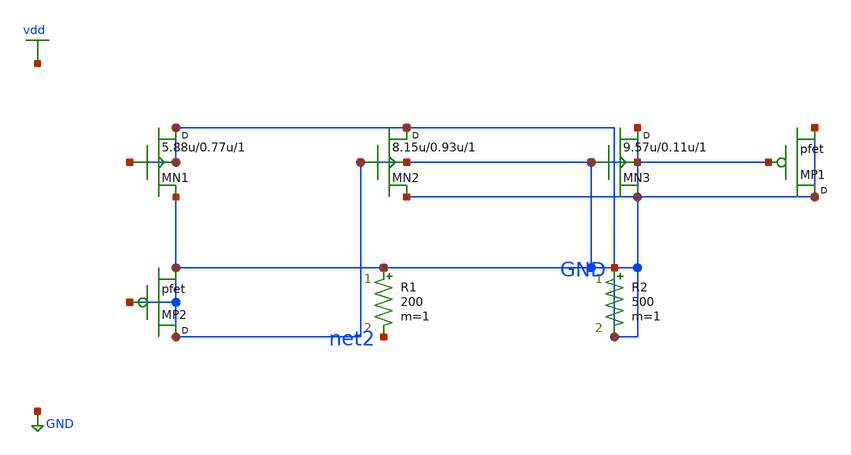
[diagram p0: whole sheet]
** sch_path: synthetic/generated/0035_synthetic.sch
**.subckt 0035_synthetic
MN1 GND GND GND GND nfet w=5.88u l=0.77u m=1
MN2 GND GND GND GND nfet w=8.15u l=0.93u m=1
MN3 GND GND GND GND nfet w=9.57u l=0.11u m=1
MP1 GND GND GND pfet m=1
MP2 GND GND GND pfet m=1
R1 GND net2 200 m=1
R2 GND GND 500 m=1
**.ends
.GLOBAL vdd
.GLOBAL GND
.end
